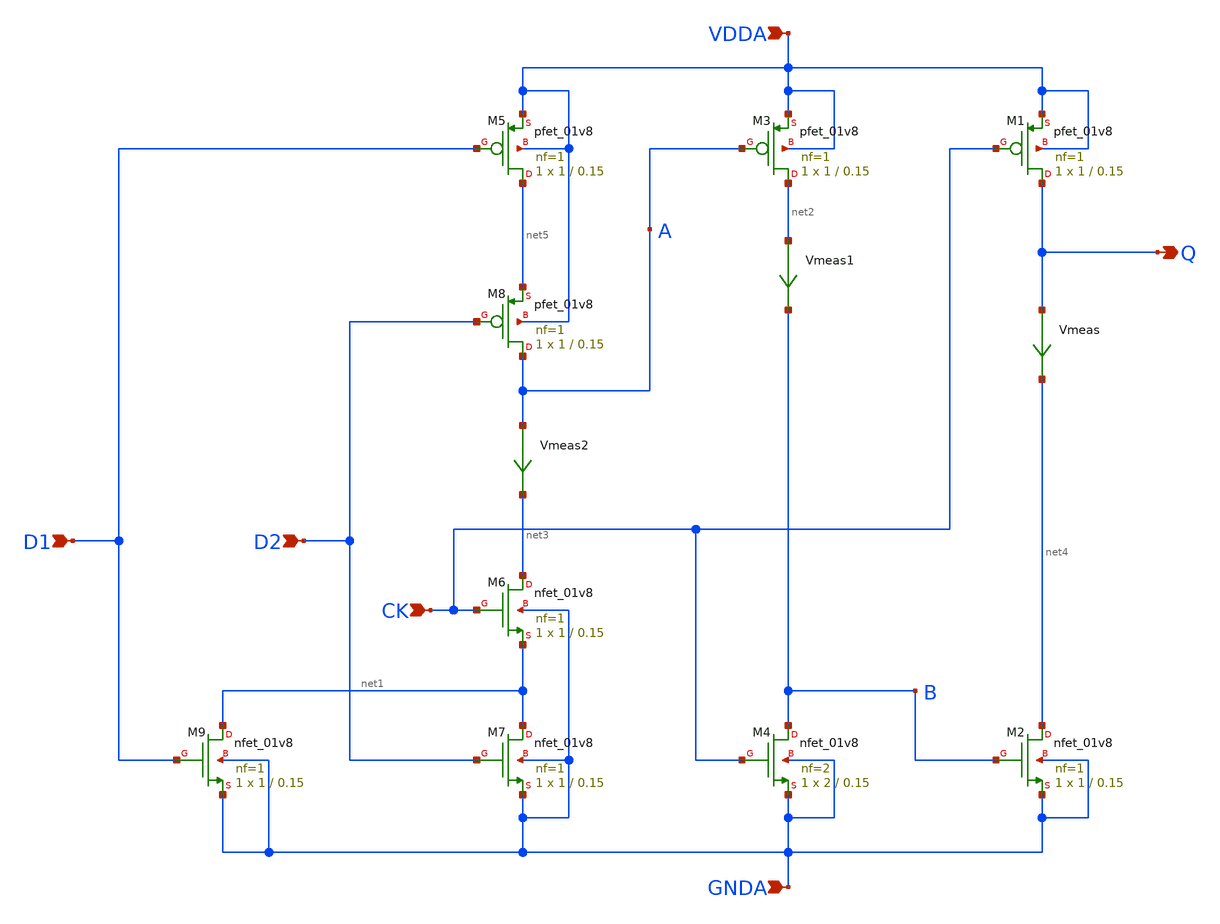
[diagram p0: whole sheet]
** sch_path: projects/pll/divider/xschem_ngspice/TSPC_FF_ratioed_nor.sch
**.subckt TSPC_FF_ratioed_nor CK D1 Q VDDA GNDA D2
*.ipin CK
*.ipin D1
*.opin Q
*.ipin VDDA
*.ipin GNDA
*.ipin D2
XM1 Q CK VDDA VDDA sky130_fd_pr__pfet_01v8 L=0.15 W=1 nf=1 ad='int((nf+1)/2) * W/nf * 0.29' as='int((nf+2)/2) * W/nf * 0.29'
+ pd='2*int((nf+1)/2) * (W/nf + 0.29)' ps='2*int((nf+2)/2) * (W/nf + 0.29)' nrd='0.29 / W' nrs='0.29 / W'
+ sa=0 sb=0 sd=0 mult=1 m=1
Vmeas Q net4 0
.save i(vmeas)
XM2 net4 B GNDA GNDA sky130_fd_pr__nfet_01v8 L=0.15 W=1 nf=1 ad='int((nf+1)/2) * W/nf * 0.29' as='int((nf+2)/2) * W/nf * 0.29'
+ pd='2*int((nf+1)/2) * (W/nf + 0.29)' ps='2*int((nf+2)/2) * (W/nf + 0.29)' nrd='0.29 / W' nrs='0.29 / W'
+ sa=0 sb=0 sd=0 mult=1 m=1
XM3 net2 A VDDA VDDA sky130_fd_pr__pfet_01v8 L=0.15 W=1 nf=1 ad='int((nf+1)/2) * W/nf * 0.29' as='int((nf+2)/2) * W/nf * 0.29'
+ pd='2*int((nf+1)/2) * (W/nf + 0.29)' ps='2*int((nf+2)/2) * (W/nf + 0.29)' nrd='0.29 / W' nrs='0.29 / W'
+ sa=0 sb=0 sd=0 mult=1 m=1
XM4 B CK GNDA GNDA sky130_fd_pr__nfet_01v8 L=0.15 W=2 nf=2 ad='int((nf+1)/2) * W/nf * 0.29' as='int((nf+2)/2) * W/nf * 0.29'
+ pd='2*int((nf+1)/2) * (W/nf + 0.29)' ps='2*int((nf+2)/2) * (W/nf + 0.29)' nrd='0.29 / W' nrs='0.29 / W'
+ sa=0 sb=0 sd=0 mult=1 m=1
Vmeas1 net2 B 0
.save i(vmeas1)
XM5 net5 D1 VDDA VDDA sky130_fd_pr__pfet_01v8 L=0.15 W=1 nf=1 ad='int((nf+1)/2) * W/nf * 0.29' as='int((nf+2)/2) * W/nf * 0.29'
+ pd='2*int((nf+1)/2) * (W/nf + 0.29)' ps='2*int((nf+2)/2) * (W/nf + 0.29)' nrd='0.29 / W' nrs='0.29 / W'
+ sa=0 sb=0 sd=0 mult=1 m=1
XM7 net1 D2 GNDA GNDA sky130_fd_pr__nfet_01v8 L=0.15 W=1 nf=1 ad='int((nf+1)/2) * W/nf * 0.29' as='int((nf+2)/2) * W/nf * 0.29'
+ pd='2*int((nf+1)/2) * (W/nf + 0.29)' ps='2*int((nf+2)/2) * (W/nf + 0.29)' nrd='0.29 / W' nrs='0.29 / W'
+ sa=0 sb=0 sd=0 mult=1 m=1
Vmeas2 A net3 0
.save i(vmeas2)
XM6 net3 CK net1 GNDA sky130_fd_pr__nfet_01v8 L=0.15 W=1 nf=1 ad='int((nf+1)/2) * W/nf * 0.29' as='int((nf+2)/2) * W/nf * 0.29'
+ pd='2*int((nf+1)/2) * (W/nf + 0.29)' ps='2*int((nf+2)/2) * (W/nf + 0.29)' nrd='0.29 / W' nrs='0.29 / W'
+ sa=0 sb=0 sd=0 mult=1 m=1
XM8 A D2 net5 VDDA sky130_fd_pr__pfet_01v8 L=0.15 W=1 nf=1 ad='int((nf+1)/2) * W/nf * 0.29' as='int((nf+2)/2) * W/nf * 0.29'
+ pd='2*int((nf+1)/2) * (W/nf + 0.29)' ps='2*int((nf+2)/2) * (W/nf + 0.29)' nrd='0.29 / W' nrs='0.29 / W'
+ sa=0 sb=0 sd=0 mult=1 m=1
XM9 net1 D1 GNDA GNDA sky130_fd_pr__nfet_01v8 L=0.15 W=1 nf=1 ad='int((nf+1)/2) * W/nf * 0.29' as='int((nf+2)/2) * W/nf * 0.29'
+ pd='2*int((nf+1)/2) * (W/nf + 0.29)' ps='2*int((nf+2)/2) * (W/nf + 0.29)' nrd='0.29 / W' nrs='0.29 / W'
+ sa=0 sb=0 sd=0 mult=1 m=1
**.ends
.end
